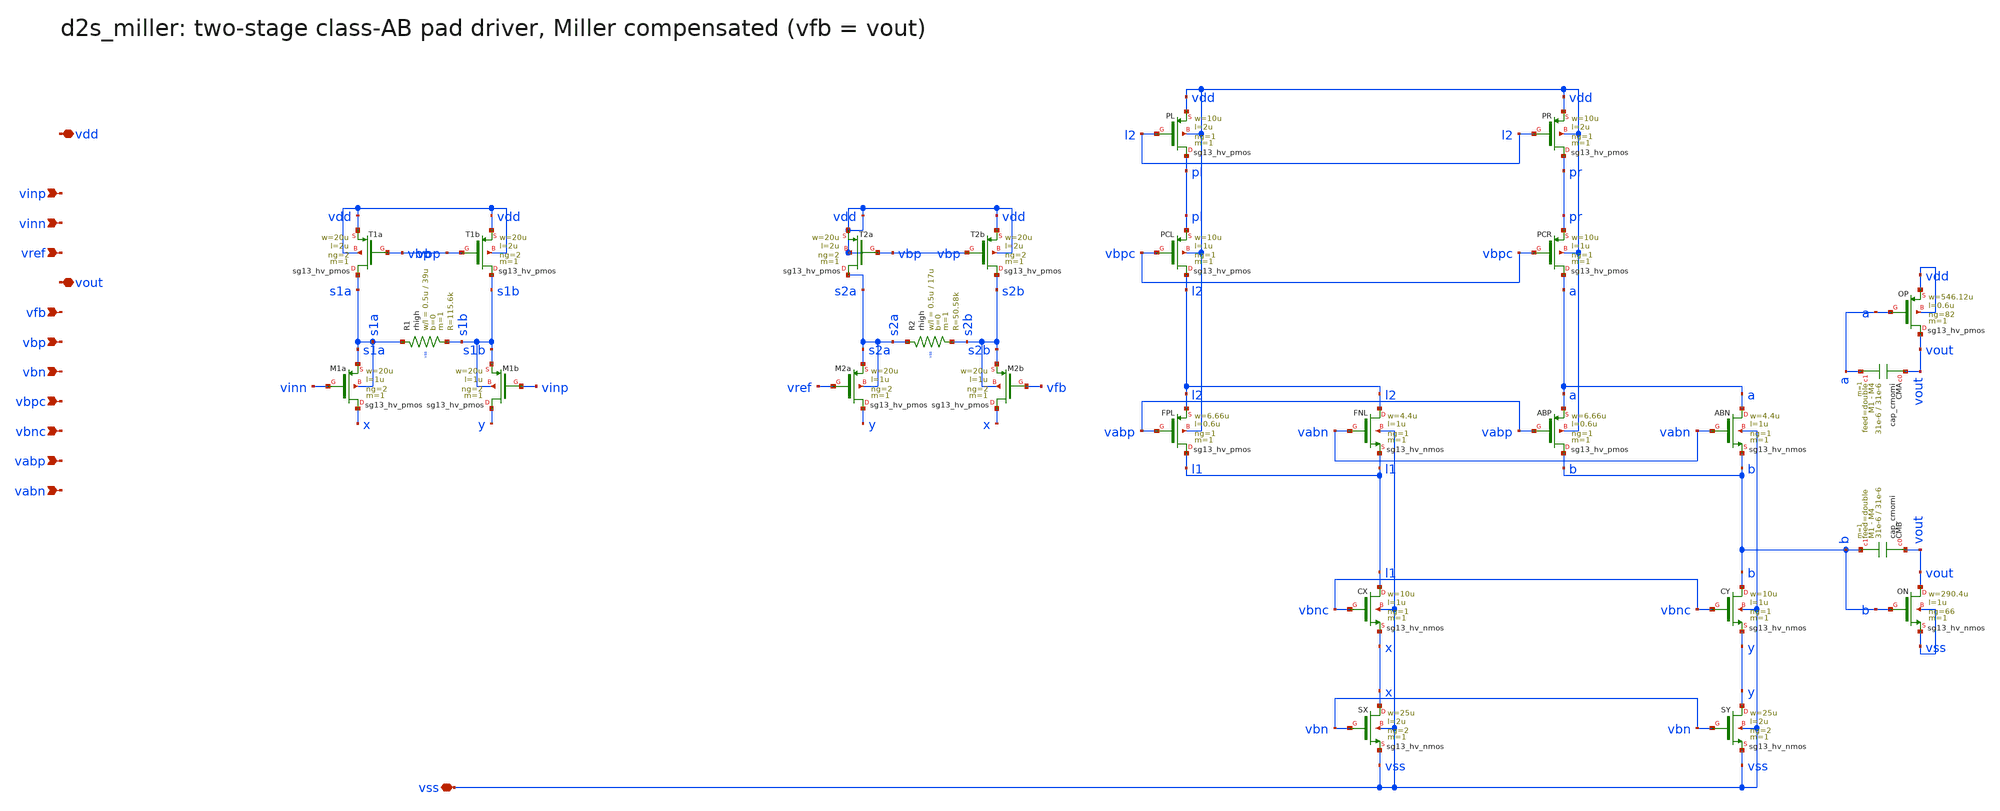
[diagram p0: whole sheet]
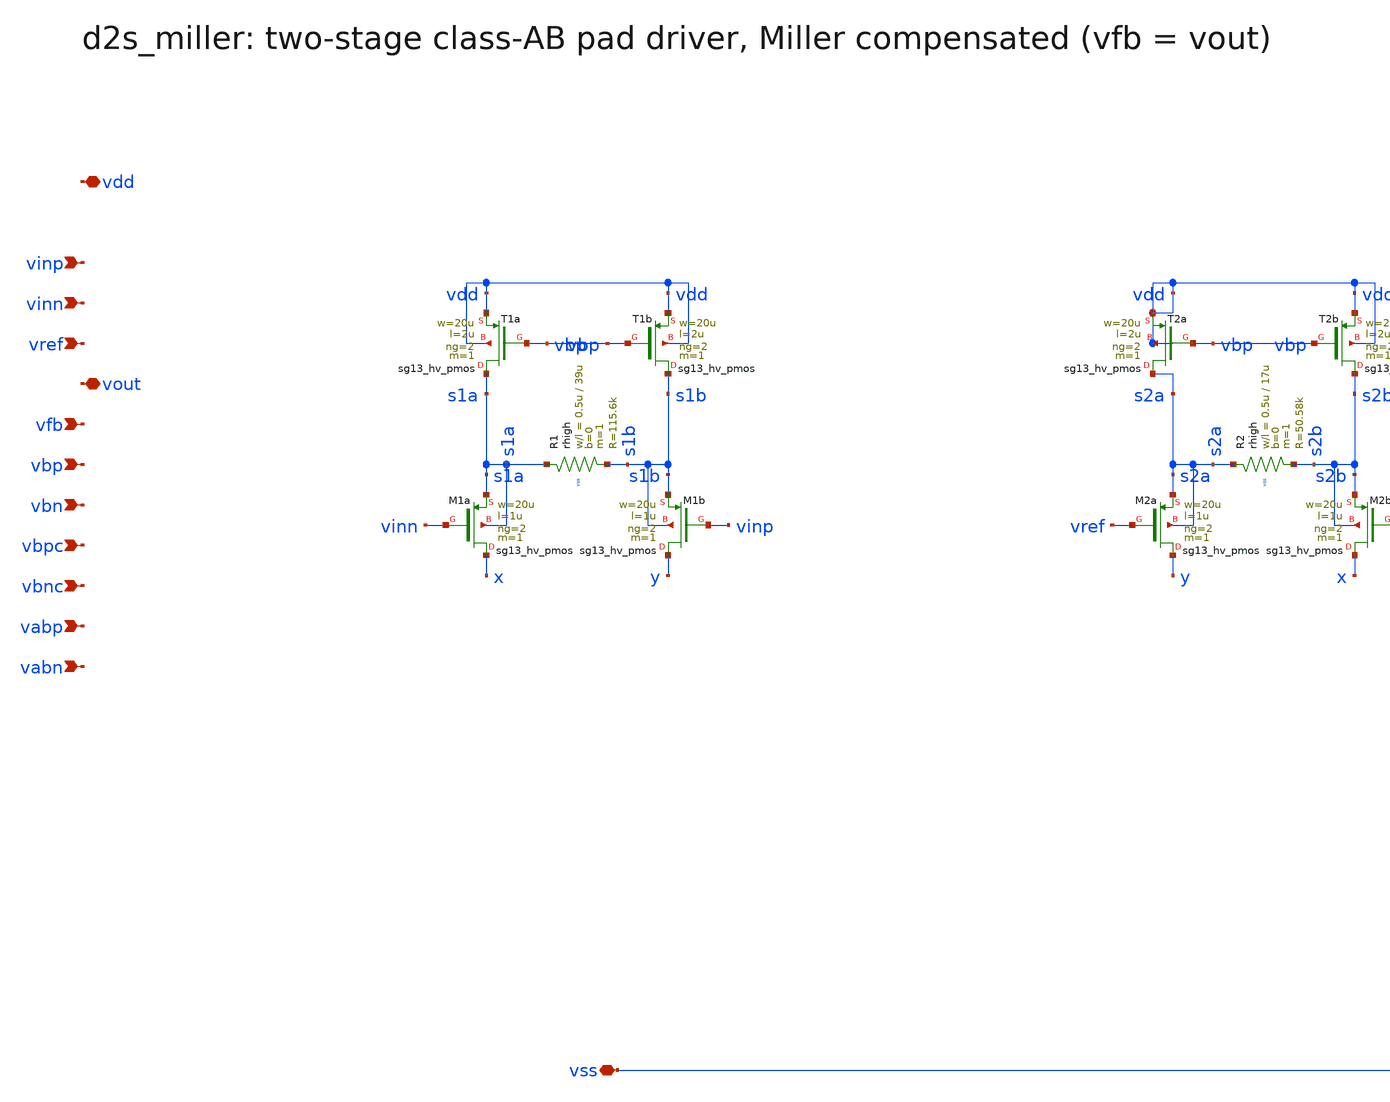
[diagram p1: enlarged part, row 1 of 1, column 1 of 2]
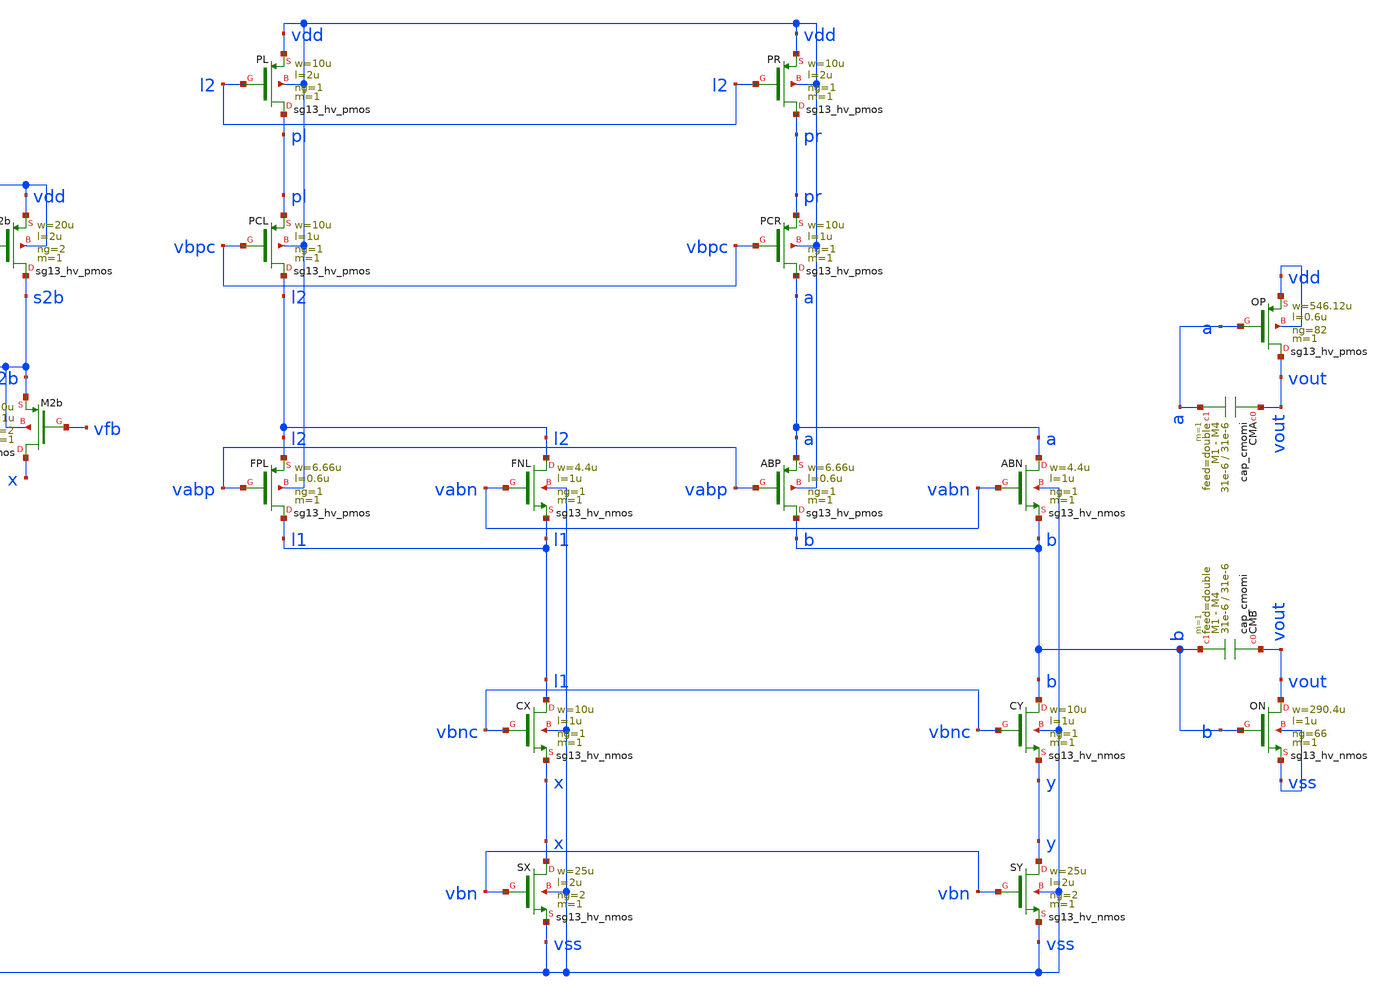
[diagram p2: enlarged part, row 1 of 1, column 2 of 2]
** sch_path: sudelbuecher/design_considerations/class_ab_pad_driver/xschem/d2s_miller.sch
**.subckt d2s_miller vdd vss vinp vinn vref vout vfb vbp vbn vbpc vbnc vabp vabn
*.iopin vdd
*.iopin vss
*.ipin vinp
*.ipin vinn
*.ipin vref
*.iopin vout
*.ipin vfb
*.ipin vbp
*.ipin vbn
*.ipin vbpc
*.ipin vbnc
*.ipin vabp
*.ipin vabn
XT1a s1a vbp vdd vdd sg13_hv_pmos w=20u l=2u ng=2 m=1 mm_ok=1
XT1b s1b vbp vdd vdd sg13_hv_pmos w=20u l=2u ng=2 m=1 mm_ok=1
XR1 s1a s1b vss rhigh w=0.5u l=39u m=1 b=0 mm_ok=1
XM1a x vinn s1a s1a sg13_hv_pmos w=20u l=1u ng=2 m=1 mm_ok=1
XM1b y vinp s1b s1b sg13_hv_pmos w=20u l=1u ng=2 m=1 mm_ok=1
XT2a s2a vbp vdd vdd sg13_hv_pmos w=20u l=2u ng=2 m=1 mm_ok=1
XT2b s2b vbp vdd vdd sg13_hv_pmos w=20u l=2u ng=2 m=1 mm_ok=1
XR2 s2a s2b vss rhigh w=0.5u l=17u m=1 b=0 mm_ok=1
XM2a y vref s2a s2a sg13_hv_pmos w=20u l=1u ng=2 m=1 mm_ok=1
XM2b x vfb s2b s2b sg13_hv_pmos w=20u l=1u ng=2 m=1 mm_ok=1
XSX x vbn vss vss sg13_hv_nmos w=25u l=2u ng=2 m=1 mm_ok=1
XSY y vbn vss vss sg13_hv_nmos w=25u l=2u ng=2 m=1 mm_ok=1
XCX l1 vbnc x vss sg13_hv_nmos w=10u l=1u ng=1 m=1 mm_ok=1
XCY b vbnc y vss sg13_hv_nmos w=10u l=1u ng=1 m=1 mm_ok=1
XFPL l1 vabp l2 vdd sg13_hv_pmos w=6.66u l=0.6u ng=1 m=1 mm_ok=1
XFNL l2 vabn l1 vss sg13_hv_nmos w=4.4u l=1u ng=1 m=1 mm_ok=1
XABP b vabp a vdd sg13_hv_pmos w=6.66u l=0.6u ng=1 m=1 mm_ok=1
XABN a vabn b vss sg13_hv_nmos w=4.4u l=1u ng=1 m=1 mm_ok=1
XOP vout a vdd vdd sg13_hv_pmos w=546.12u l=0.6u ng=82 m=1 mm_ok=1
XON vout b vss vss sg13_hv_nmos w=290.4u l=1u ng=66 m=1 mm_ok=1
XCMA vout a cap_cmomi w=31e-6 l=31e-6 mmin=1 mmax=4 feed=double subblock=0 m=1 mm_ok=1
XCMB vout b cap_cmomi w=31e-6 l=31e-6 mmin=1 mmax=4 feed=double subblock=0 m=1 mm_ok=1
XPL pl l2 vdd vdd sg13_hv_pmos w=10u l=2u ng=1 m=1 mm_ok=1
XPR pr l2 vdd vdd sg13_hv_pmos w=10u l=2u ng=1 m=1 mm_ok=1
XPCL l2 vbpc pl vdd sg13_hv_pmos w=10u l=1u ng=1 m=1 mm_ok=1
XPCR a vbpc pr vdd sg13_hv_pmos w=10u l=1u ng=1 m=1 mm_ok=1
**.ends
.end
